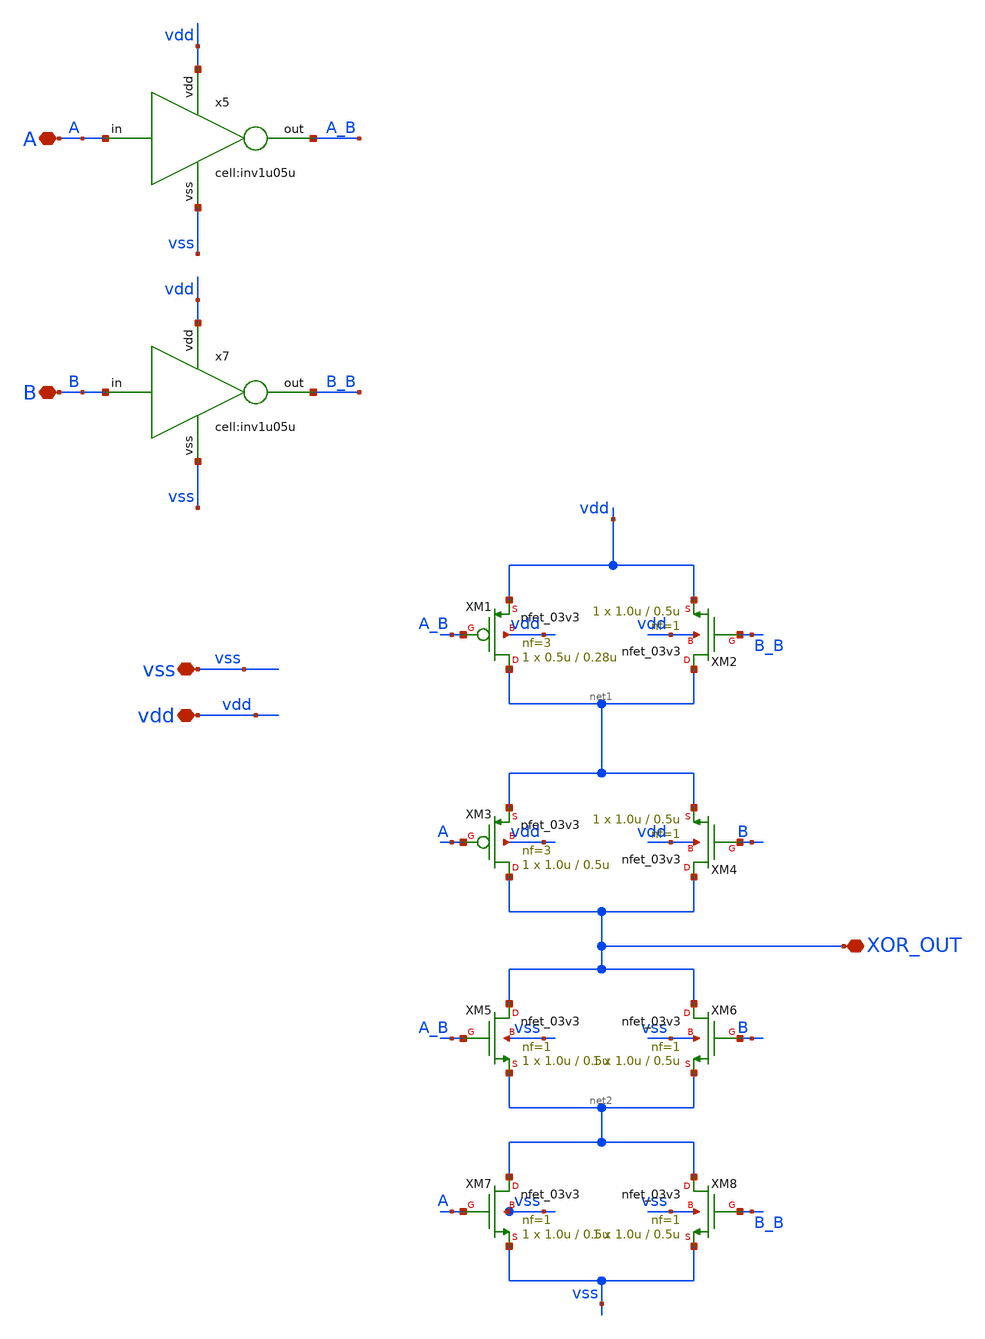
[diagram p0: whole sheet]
** sch_path: designs/libs/xp_core_analog/2_XOR.sch
**.subckt 2_XOR vdd vss XOR_OUT B A
*.iopin vdd
*.iopin vss
*.iopin XOR_OUT
*.iopin B
*.iopin A
XM1 net1 A_B vdd vdd pfet_03v3 L=0.28u W=0.5u nf=3 ad='int((nf+1)/2) * W/nf * 0.18u' as='int((nf+2)/2) * W/nf * 0.18u'
+ pd='2*int((nf+1)/2) * (W/nf + 0.18u)' ps='2*int((nf+2)/2) * (W/nf + 0.18u)' nrd='0.18u / W' nrs='0.18u / W'
+ sa=0 sb=0 sd=0 m=1
XM2 net1 B_B vdd vdd nfet_03v3 L=0.5u W=1.0u nf=1 ad='int((nf+1)/2) * W/nf * 0.18u' as='int((nf+2)/2) * W/nf * 0.18u'
+ pd='2*int((nf+1)/2) * (W/nf + 0.18u)' ps='2*int((nf+2)/2) * (W/nf + 0.18u)' nrd='0.18u / W' nrs='0.18u / W'
+ sa=0 sb=0 sd=0 m=1
x7 B vdd B_B vss inv1u05u
x5 A vdd A_B vss inv1u05u
XM3 XOR_OUT A net1 vdd pfet_03v3 L=0.5u W=1.0u nf=3 ad='int((nf+1)/2) * W/nf * 0.18u' as='int((nf+2)/2) * W/nf * 0.18u'
+ pd='2*int((nf+1)/2) * (W/nf + 0.18u)' ps='2*int((nf+2)/2) * (W/nf + 0.18u)' nrd='0.18u / W' nrs='0.18u / W'
+ sa=0 sb=0 sd=0 m=1
XM4 XOR_OUT B net1 vdd nfet_03v3 L=0.5u W=1.0u nf=1 ad='int((nf+1)/2) * W/nf * 0.18u' as='int((nf+2)/2) * W/nf * 0.18u'
+ pd='2*int((nf+1)/2) * (W/nf + 0.18u)' ps='2*int((nf+2)/2) * (W/nf + 0.18u)' nrd='0.18u / W' nrs='0.18u / W'
+ sa=0 sb=0 sd=0 m=1
XM5 XOR_OUT A_B net2 vss nfet_03v3 L=0.5u W=1.0u nf=1 ad='int((nf+1)/2) * W/nf * 0.18u' as='int((nf+2)/2) * W/nf * 0.18u'
+ pd='2*int((nf+1)/2) * (W/nf + 0.18u)' ps='2*int((nf+2)/2) * (W/nf + 0.18u)' nrd='0.18u / W' nrs='0.18u / W'
+ sa=0 sb=0 sd=0 m=1
XM6 XOR_OUT B net2 vss nfet_03v3 L=0.5u W=1.0u nf=1 ad='int((nf+1)/2) * W/nf * 0.18u' as='int((nf+2)/2) * W/nf * 0.18u'
+ pd='2*int((nf+1)/2) * (W/nf + 0.18u)' ps='2*int((nf+2)/2) * (W/nf + 0.18u)' nrd='0.18u / W' nrs='0.18u / W'
+ sa=0 sb=0 sd=0 m=1
XM7 net2 A vss vss nfet_03v3 L=0.5u W=1.0u nf=1 ad='int((nf+1)/2) * W/nf * 0.18u' as='int((nf+2)/2) * W/nf * 0.18u'
+ pd='2*int((nf+1)/2) * (W/nf + 0.18u)' ps='2*int((nf+2)/2) * (W/nf + 0.18u)' nrd='0.18u / W' nrs='0.18u / W'
+ sa=0 sb=0 sd=0 m=1
XM8 net2 B_B vss vss nfet_03v3 L=0.5u W=1.0u nf=1 ad='int((nf+1)/2) * W/nf * 0.18u' as='int((nf+2)/2) * W/nf * 0.18u'
+ pd='2*int((nf+1)/2) * (W/nf + 0.18u)' ps='2*int((nf+2)/2) * (W/nf + 0.18u)' nrd='0.18u / W' nrs='0.18u / W'
+ sa=0 sb=0 sd=0 m=1
**.ends
.end
